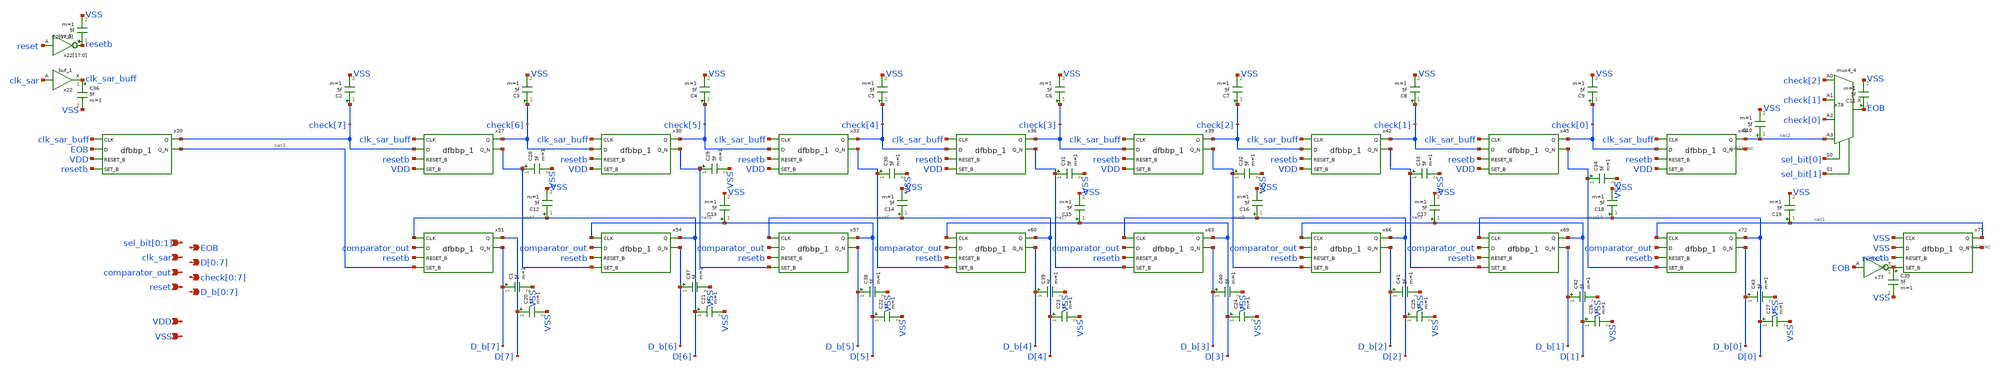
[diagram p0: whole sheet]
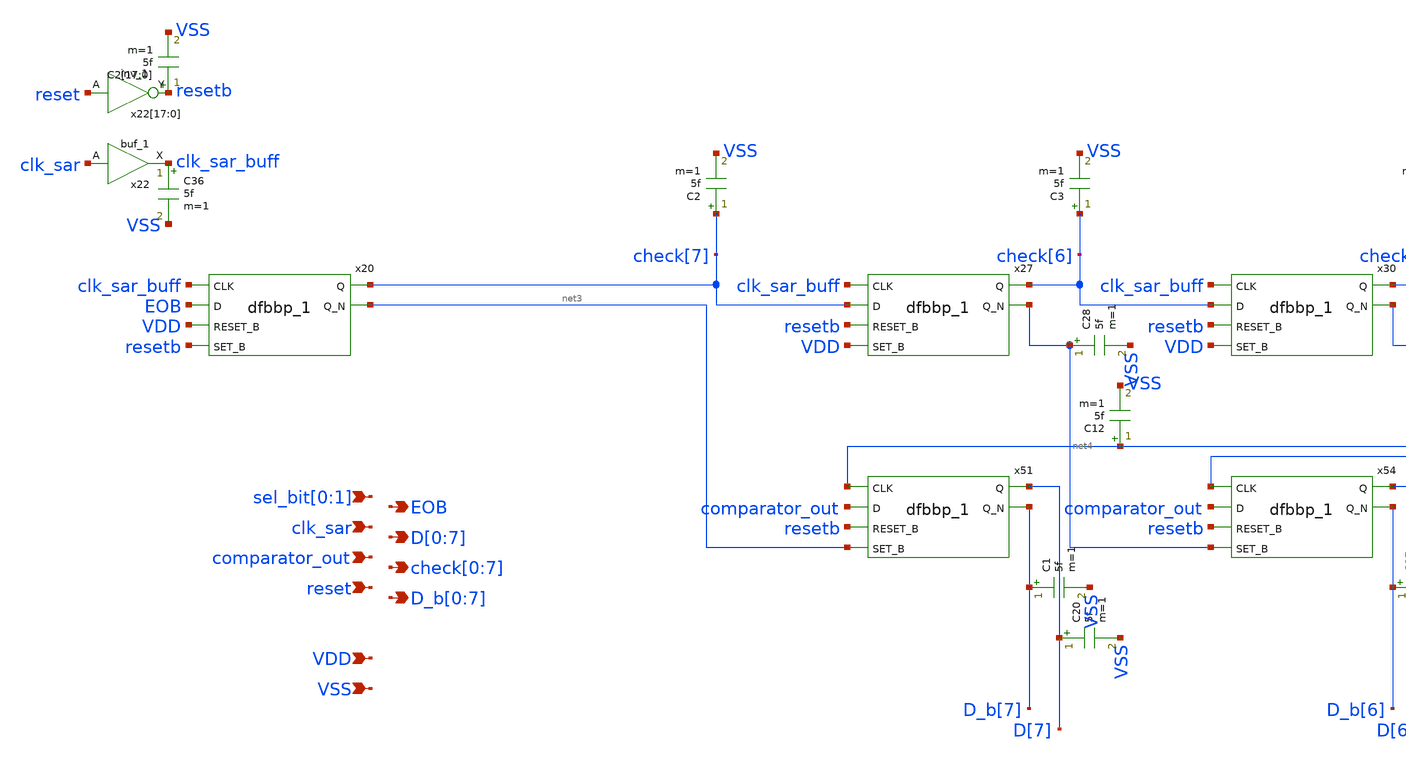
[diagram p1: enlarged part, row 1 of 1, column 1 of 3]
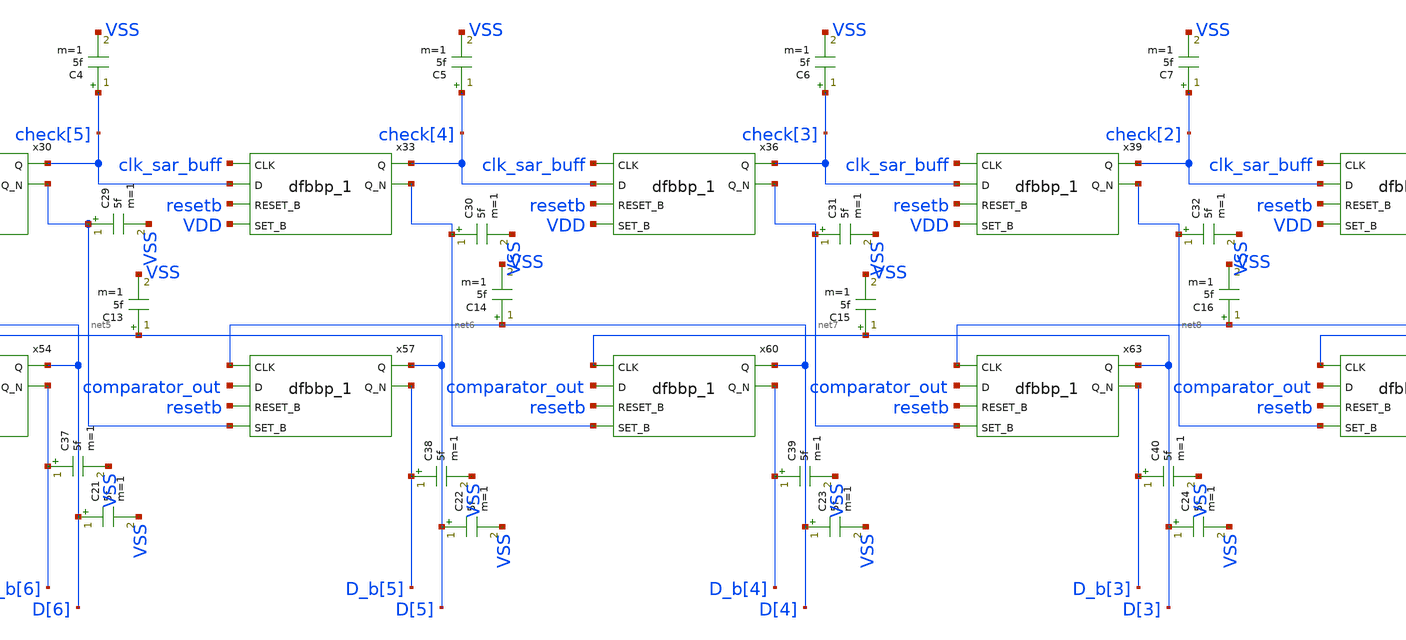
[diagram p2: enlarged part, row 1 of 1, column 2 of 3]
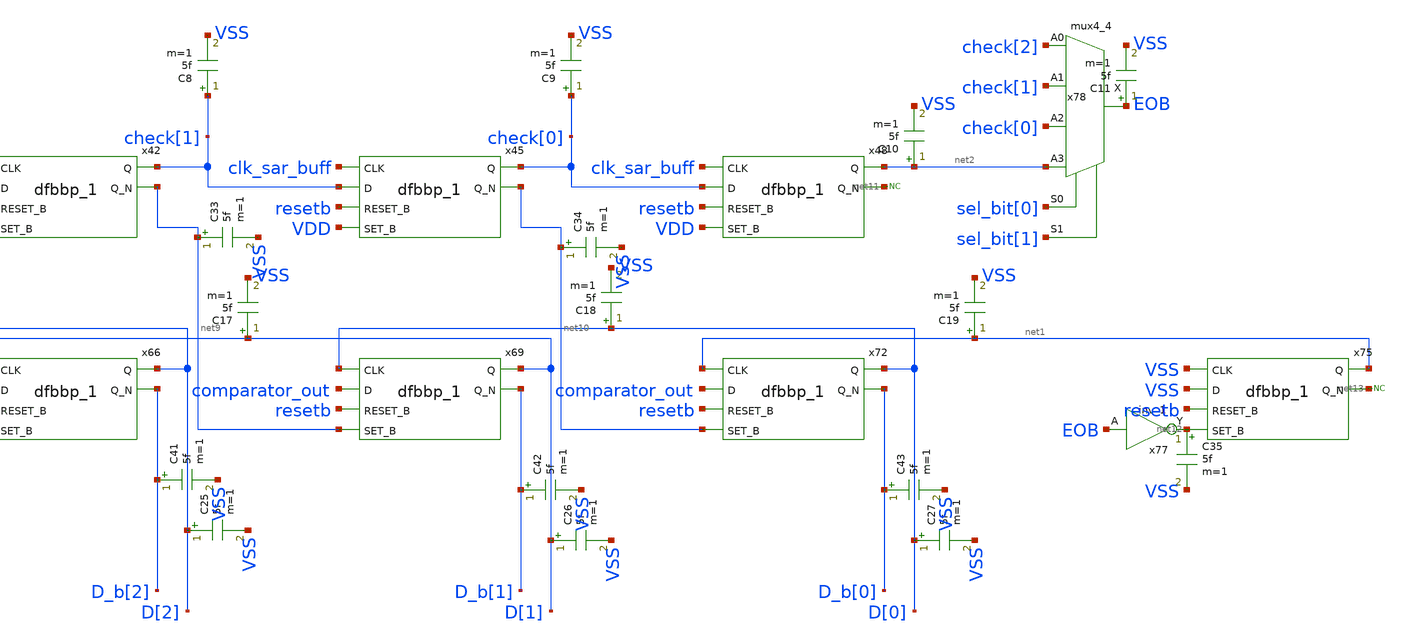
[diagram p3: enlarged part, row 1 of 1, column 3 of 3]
** sch_path: hgu/xschem/hgu_sarlogic_8bit_logic.sch
**.subckt hgu_sarlogic_8bit_logic clk_sar VDD VSS comparator_out reset EOB
*+ D[0],D[1],D[2],D[3],D[4],D[5],D[6],D[7] check[0],check[1],check[2],check[3],check[4],check[5],check[6],check[7] sel_bit[0],sel_bit[1]
*+ D_b[0],D_b[1],D_b[2],D_b[3],D_b[4],D_b[5],D_b[6],D_b[7]
*.ipin clk_sar
*.ipin VDD
*.ipin VSS
*.ipin comparator_out
*.ipin reset
*.opin EOB
*.opin D[0],D[1],D[2],D[3],D[4],D[5],D[6],D[7]
*.opin check[0],check[1],check[2],check[3],check[4],check[5],check[6],check[7]
*.ipin sel_bit[0],sel_bit[1]
*.opin D_b[0],D_b[1],D_b[2],D_b[3],D_b[4],D_b[5],D_b[6],D_b[7]
x20 clk_sar_buff EOB VDD resetb VGND VNB VPB VPWR check[7] net3 sky130_fd_sc_hd__dfbbp_1
x27 clk_sar_buff check[7] resetb VDD VGND VNB VPB VPWR check[6] net4 sky130_fd_sc_hd__dfbbp_1
x30 clk_sar_buff check[6] resetb VDD VGND VNB VPB VPWR check[5] net5 sky130_fd_sc_hd__dfbbp_1
x33 clk_sar_buff check[5] resetb VDD VGND VNB VPB VPWR check[4] net6 sky130_fd_sc_hd__dfbbp_1
x36 clk_sar_buff check[4] resetb VDD VGND VNB VPB VPWR check[3] net7 sky130_fd_sc_hd__dfbbp_1
x39 clk_sar_buff check[3] resetb VDD VGND VNB VPB VPWR check[2] net8 sky130_fd_sc_hd__dfbbp_1
x42 clk_sar_buff check[2] resetb VDD VGND VNB VPB VPWR check[1] net9 sky130_fd_sc_hd__dfbbp_1
x45 clk_sar_buff check[1] resetb VDD VGND VNB VPB VPWR check[0] net10 sky130_fd_sc_hd__dfbbp_1
x48 clk_sar_buff check[0] resetb VDD VGND VNB VPB VPWR net2 net11 sky130_fd_sc_hd__dfbbp_1
x51 D[6] comparator_out resetb net3 VGND VNB VPB VPWR D[7] D_b[7] sky130_fd_sc_hd__dfbbp_1
x54 D[5] comparator_out resetb net4 VGND VNB VPB VPWR D[6] D_b[6] sky130_fd_sc_hd__dfbbp_1
x57 D[4] comparator_out resetb net5 VGND VNB VPB VPWR D[5] D_b[5] sky130_fd_sc_hd__dfbbp_1
x60 D[3] comparator_out resetb net6 VGND VNB VPB VPWR D[4] D_b[4] sky130_fd_sc_hd__dfbbp_1
x63 D[2] comparator_out resetb net7 VGND VNB VPB VPWR D[3] D_b[3] sky130_fd_sc_hd__dfbbp_1
x66 D[1] comparator_out resetb net8 VGND VNB VPB VPWR D[2] D_b[2] sky130_fd_sc_hd__dfbbp_1
x69 D[0] comparator_out resetb net9 VGND VNB VPB VPWR D[1] D_b[1] sky130_fd_sc_hd__dfbbp_1
x72 net1 comparator_out resetb net10 VGND VNB VPB VPWR D[0] D_b[0] sky130_fd_sc_hd__dfbbp_1
x75 VSS VSS resetb net12 VGND VNB VPB VPWR net1 net13 sky130_fd_sc_hd__dfbbp_1
x77 EOB VGND VNB VPB VPWR net12 sky130_fd_sc_hd__inv_1
* noconn #net13
x78 check[2] check[1] check[0] net2 sel_bit[0] sel_bit[1] VGND VNB VPB VPWR EOB
+ sky130_fd_sc_hd__mux4_4
* noconn #net11
x22[17] reset VGND VNB VPB VPWR resetb sky130_fd_sc_hd__inv_1
x22[16] reset VGND VNB VPB VPWR resetb sky130_fd_sc_hd__inv_1
x22[15] reset VGND VNB VPB VPWR resetb sky130_fd_sc_hd__inv_1
x22[14] reset VGND VNB VPB VPWR resetb sky130_fd_sc_hd__inv_1
x22[13] reset VGND VNB VPB VPWR resetb sky130_fd_sc_hd__inv_1
x22[12] reset VGND VNB VPB VPWR resetb sky130_fd_sc_hd__inv_1
x22[11] reset VGND VNB VPB VPWR resetb sky130_fd_sc_hd__inv_1
x22[10] reset VGND VNB VPB VPWR resetb sky130_fd_sc_hd__inv_1
x22[9] reset VGND VNB VPB VPWR resetb sky130_fd_sc_hd__inv_1
x22[8] reset VGND VNB VPB VPWR resetb sky130_fd_sc_hd__inv_1
x22[7] reset VGND VNB VPB VPWR resetb sky130_fd_sc_hd__inv_1
x22[6] reset VGND VNB VPB VPWR resetb sky130_fd_sc_hd__inv_1
x22[5] reset VGND VNB VPB VPWR resetb sky130_fd_sc_hd__inv_1
x22[4] reset VGND VNB VPB VPWR resetb sky130_fd_sc_hd__inv_1
x22[3] reset VGND VNB VPB VPWR resetb sky130_fd_sc_hd__inv_1
x22[2] reset VGND VNB VPB VPWR resetb sky130_fd_sc_hd__inv_1
x22[1] reset VGND VNB VPB VPWR resetb sky130_fd_sc_hd__inv_1
x22[0] reset VGND VNB VPB VPWR resetb sky130_fd_sc_hd__inv_1
x22 clk_sar VGND VNB VPB VPWR clk_sar_buff sky130_fd_sc_hd__buf_1
C2[17] resetb VSS 5f m=1
C2[16] resetb VSS 5f m=1
C2[15] resetb VSS 5f m=1
C2[14] resetb VSS 5f m=1
C2[13] resetb VSS 5f m=1
C2[12] resetb VSS 5f m=1
C2[11] resetb VSS 5f m=1
C2[10] resetb VSS 5f m=1
C2[9] resetb VSS 5f m=1
C2[8] resetb VSS 5f m=1
C2[7] resetb VSS 5f m=1
C2[6] resetb VSS 5f m=1
C2[5] resetb VSS 5f m=1
C2[4] resetb VSS 5f m=1
C2[3] resetb VSS 5f m=1
C2[2] resetb VSS 5f m=1
C2[1] resetb VSS 5f m=1
C2[0] resetb VSS 5f m=1
C2 check[7] VSS 5f m=1
C3 check[6] VSS 5f m=1
C4 check[5] VSS 5f m=1
C5 check[4] VSS 5f m=1
C6 check[3] VSS 5f m=1
C7 check[2] VSS 5f m=1
C8 check[1] VSS 5f m=1
C9 check[0] VSS 5f m=1
C10 net2 VSS 5f m=1
C11 EOB VSS 5f m=1
C12 D[6] VSS 5f m=1
C13 D[5] VSS 5f m=1
C14 D[4] VSS 5f m=1
C15 D[3] VSS 5f m=1
C16 D[2] VSS 5f m=1
C17 D[1] VSS 5f m=1
C18 D[0] VSS 5f m=1
C19 net1 VSS 5f m=1
C20 D[7] VSS 5f m=1
C21 D[6] VSS 5f m=1
C22 D[5] VSS 5f m=1
C23 D[4] VSS 5f m=1
C24 D[3] VSS 5f m=1
C25 D[2] VSS 5f m=1
C26 D[1] VSS 5f m=1
C27 D[0] VSS 5f m=1
C28 net4 VSS 5f m=1
C29 net5 VSS 5f m=1
C30 net6 VSS 5f m=1
C31 net7 VSS 5f m=1
C32 net8 VSS 5f m=1
C33 net9 VSS 5f m=1
C34 net10 VSS 5f m=1
C35 net12 VSS 5f m=1
C36 clk_sar_buff VSS 5f m=1
C1 D_b[7] VSS 5f m=1
C37 D_b[6] VSS 5f m=1
C38 D_b[5] VSS 5f m=1
C39 D_b[4] VSS 5f m=1
C40 D_b[3] VSS 5f m=1
C41 D_b[2] VSS 5f m=1
C42 D_b[1] VSS 5f m=1
C43 D_b[0] VSS 5f m=1
**.ends
.end
